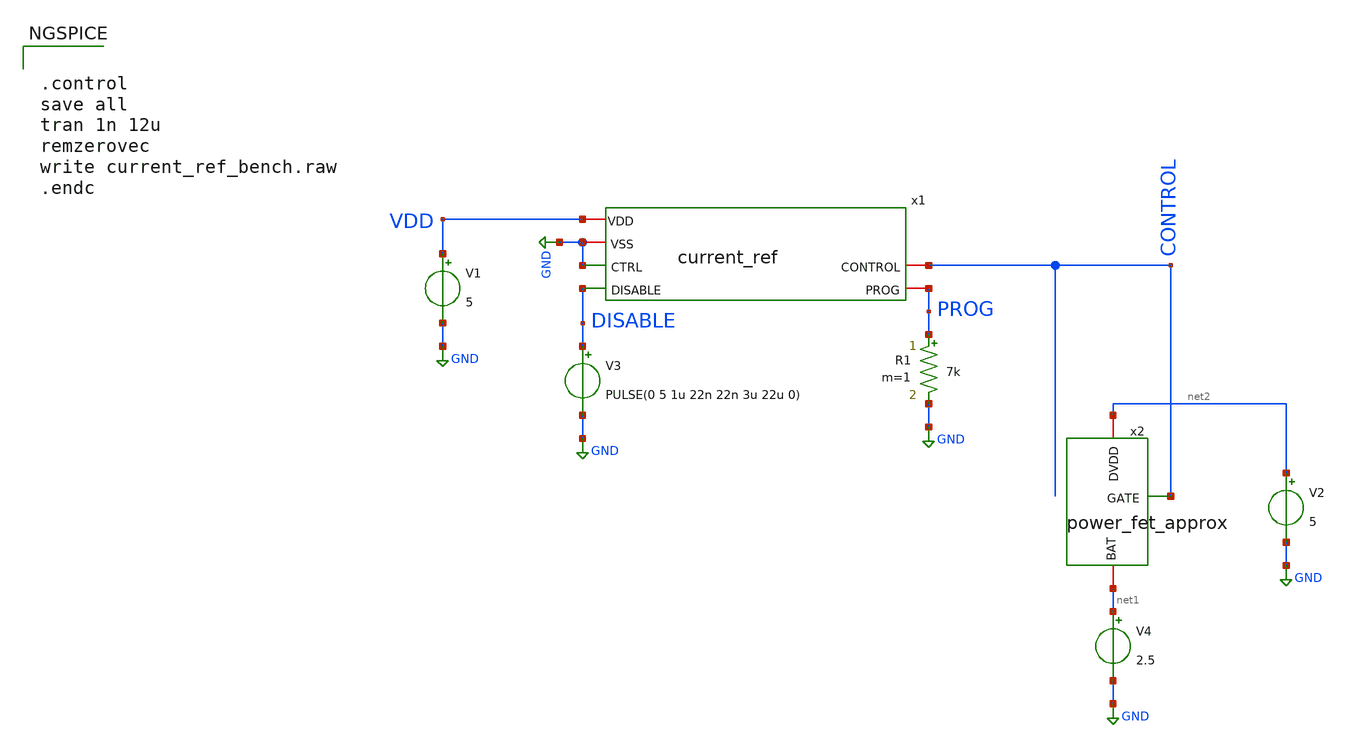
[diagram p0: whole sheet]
** sch_path: analog/xschem/current_ref_bench.sch
**.subckt current_ref_bench
V1 VDD GND 5
V4 net1 GND 2.5
V2 net2 GND 5
R1 PROG GND 7k m=1
V3 DISABLE GND PULSE(0 5 1u 22n 22n 3u 22u 0)
x2 net2 CONTROL net1 power_fet_approx
x1 VDD GND CONTROL PROG GND DISABLE current_ref
**** begin user architecture code


.control
save all
tran 1n 12u
remzerovec
write current_ref_bench.raw
.endc



.include $::180MCU_MODELS/design.ngspice
.lib $::180MCU_MODELS/sm141064.ngspice typical
.lib $::180MCU_MODELS/sm141064.ngspice res_typical
.lib $::180MCU_MODELS/sm141064.ngspice diode_typical
.lib $::180MCU_MODELS/sm141064.ngspice mimcap_typical
.lib $::180MCU_MODELS/sm141064.ngspice cap_mim

**** end user architecture code
**.ends
.GLOBAL GND
.end
